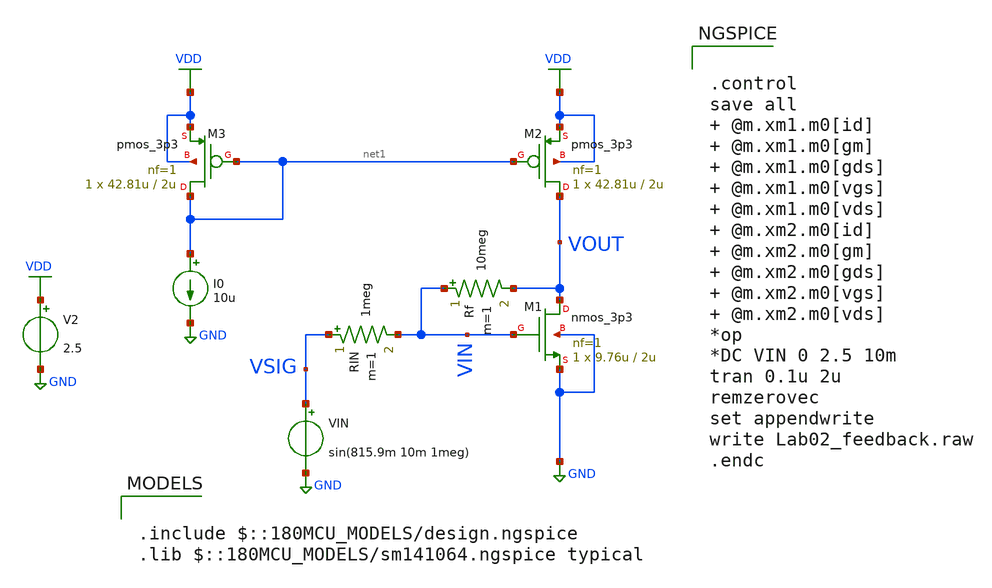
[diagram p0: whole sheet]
** sch_path: ITI_Labs/Lab2/Design/Lab02_feedback.sch
**.subckt Lab02_feedback
XM1 VOUT VIN GND GND nmos_3p3 L=2u W=9.76u nf=1 ad='int((nf+1)/2) * W/nf * 0.18u' as='int((nf+2)/2) * W/nf * 0.18u'
+ pd='2*int((nf+1)/2) * (W/nf + 0.18u)' ps='2*int((nf+2)/2) * (W/nf + 0.18u)' nrd='0.18u / W' nrs='0.18u / W'
+ sa=0 sb=0 sd=0 m=1
VIN VSIG GND sin(815.9m 10m 1meg)
V2 VDD GND 2.5
Rf VIN VOUT 10meg m=1
RIN VSIG VIN 1meg m=1
XM2 VOUT net1 VDD VDD pmos_3p3 L=2u W=42.81u nf=1 ad='int((nf+1)/2) * W/nf * 0.18u' as='int((nf+2)/2) * W/nf * 0.18u'
+ pd='2*int((nf+1)/2) * (W/nf + 0.18u)' ps='2*int((nf+2)/2) * (W/nf + 0.18u)' nrd='0.18u / W' nrs='0.18u / W'
+ sa=0 sb=0 sd=0 m=1
I0 net1 GND 10u
XM3 net1 net1 VDD VDD pmos_3p3 L=2u W=42.81u nf=1 ad='int((nf+1)/2) * W/nf * 0.18u' as='int((nf+2)/2) * W/nf * 0.18u'
+ pd='2*int((nf+1)/2) * (W/nf + 0.18u)' ps='2*int((nf+2)/2) * (W/nf + 0.18u)' nrd='0.18u / W' nrs='0.18u / W'
+ sa=0 sb=0 sd=0 m=1
**** begin user architecture code

.include $::180MCU_MODELS/design.ngspice
.lib $::180MCU_MODELS/sm141064.ngspice typical



.control
save all  @m.xm1.m0[id]  @m.xm1.m0[gm]  @m.xm1.m0[gds]  @m.xm1.m0[vgs]  @m.xm1.m0[vds]
+  @m.xm2.m0[id]  @m.xm2.m0[gm]  @m.xm2.m0[gds]  @m.xm2.m0[vgs]  @m.xm2.m0[vds]
*op
*DC VIN 0 2.5 10m
tran 0.1u 2u
remzerovec
set appendwrite
write Lab02_feedback.raw
.endc


**** end user architecture code
**.ends
.GLOBAL GND
.GLOBAL VDD
.end
